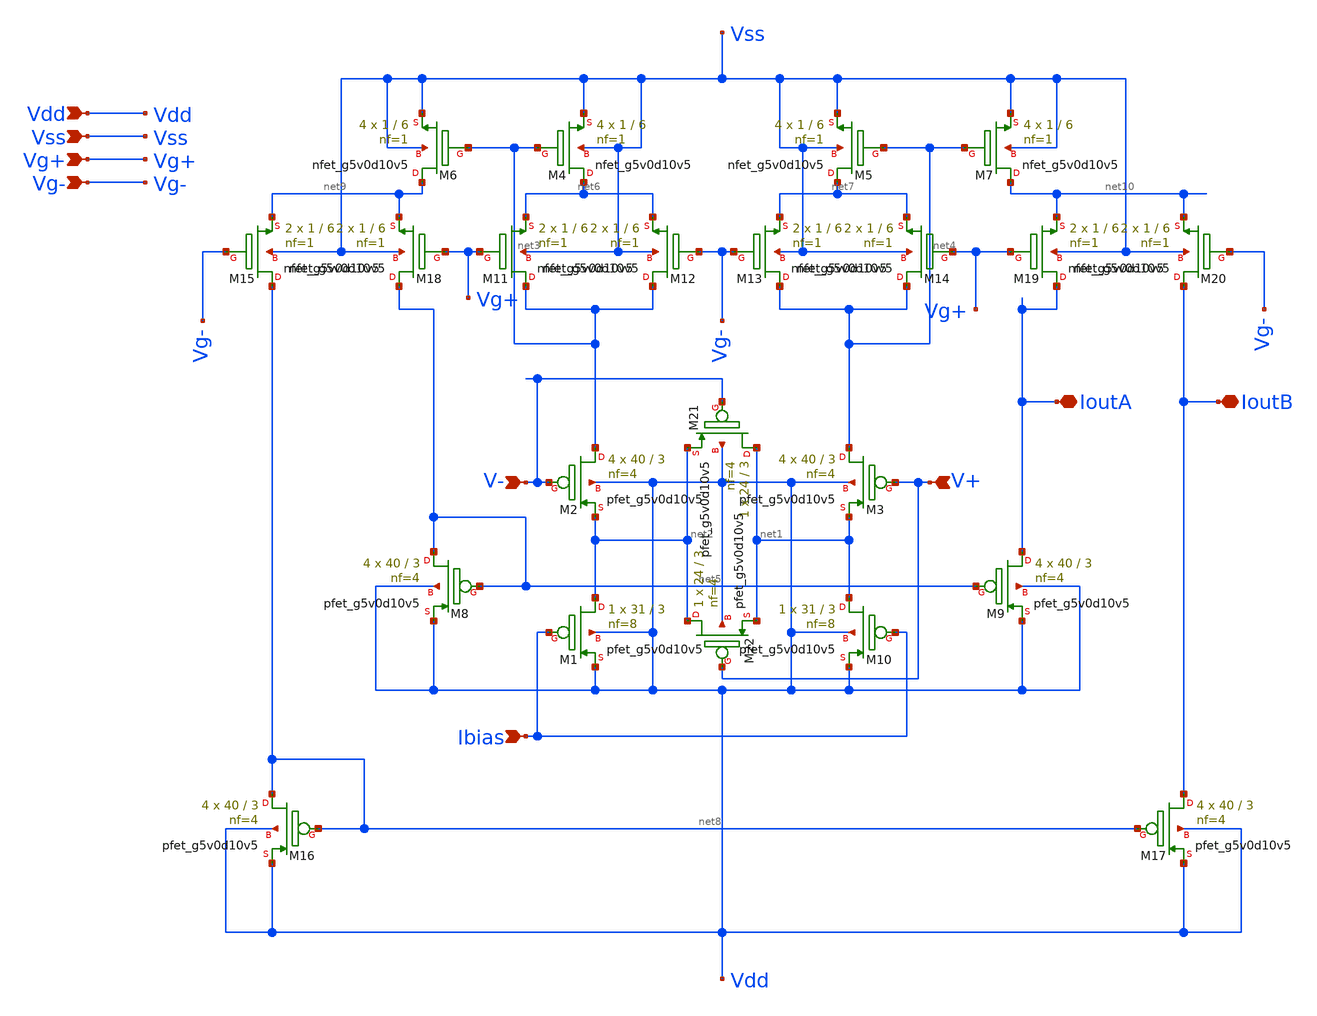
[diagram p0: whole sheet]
** sch_path: xschem/Gm_C_LPF.sch
**.subckt Gm_C_LPF V- V+ Vdd Vss Ibias Vg- Vg+ IoutA IoutB
*.ipin V-
*.ipin V+
*.ipin Vdd
*.ipin Vss
*.ipin Ibias
*.ipin Vg-
*.ipin Vg+
*.iopin IoutA
*.iopin IoutB
XM1 net2 Ibias Vdd Vdd sky130_fd_pr__pfet_g5v0d10v5 L=3 W=31 nf=8 ad='int((8 + 1)/2) * 31 / 8 * 0.29'
+ as='int((8 + 2)/2) * 31 / 8 * 0.29' pd='2*int((8 + 1)/2) * (31 / 8 + 0.29)' ps='2*int((8 + 2)/2) * (31 / 8 + 0.29)'
+ nrd='0.29 / 31 ' nrs='0.29 / 31 ' sa=0 sb=0 sd=0 mult=1 m=1
XM2 net3 V- net2 Vdd sky130_fd_pr__pfet_g5v0d10v5 L=3 W=40 nf=4 ad='int((4 + 1)/2) * 40 / 4 * 0.29' as='int((4 + 2)/2) * 40 / 4 * 0.29'
+ pd='2*int((4 + 1)/2) * (40 / 4 + 0.29)' ps='2*int((4 + 2)/2) * (40 / 4 + 0.29)' nrd='0.29 / 40 ' nrs='0.29 / 40 '
+ sa=0 sb=0 sd=0 mult=4 m=4
XM3 net4 V+ net1 Vdd sky130_fd_pr__pfet_g5v0d10v5 L=3 W=40 nf=4 ad='int((4 + 1)/2) * 40 / 4 * 0.29' as='int((4 + 2)/2) * 40 / 4 * 0.29'
+ pd='2*int((4 + 1)/2) * (40 / 4 + 0.29)' ps='2*int((4 + 2)/2) * (40 / 4 + 0.29)' nrd='0.29 / 40 ' nrs='0.29 / 40 '
+ sa=0 sb=0 sd=0 mult=4 m=4
XM4 net6 net3 Vss Vss sky130_fd_pr__nfet_g5v0d10v5 L=6 W=1 nf=1 ad='int((1 + 1)/2) * 1 / 1 * 0.29' as='int((1 + 2)/2) * 1 / 1 * 0.29'
+ pd='2*int((1 + 1)/2) * (1 / 1 + 0.29)' ps='2*int((1 + 2)/2) * (1 / 1 + 0.29)' nrd='0.29 / 1 ' nrs='0.29 / 1 '
+ sa=0 sb=0 sd=0 mult=4 m=4
XM5 net7 net4 Vss Vss sky130_fd_pr__nfet_g5v0d10v5 L=6 W=1 nf=1 ad='int((1 + 1)/2) * 1 / 1 * 0.29' as='int((1 + 2)/2) * 1 / 1 * 0.29'
+ pd='2*int((1 + 1)/2) * (1 / 1 + 0.29)' ps='2*int((1 + 2)/2) * (1 / 1 + 0.29)' nrd='0.29 / 1 ' nrs='0.29 / 1 '
+ sa=0 sb=0 sd=0 mult=4 m=4
XM6 net9 net3 Vss Vss sky130_fd_pr__nfet_g5v0d10v5 L=6 W=1 nf=1 ad='int((1 + 1)/2) * 1 / 1 * 0.29' as='int((1 + 2)/2) * 1 / 1 * 0.29'
+ pd='2*int((1 + 1)/2) * (1 / 1 + 0.29)' ps='2*int((1 + 2)/2) * (1 / 1 + 0.29)' nrd='0.29 / 1 ' nrs='0.29 / 1 '
+ sa=0 sb=0 sd=0 mult=4 m=4
XM7 net10 net4 Vss Vss sky130_fd_pr__nfet_g5v0d10v5 L=6 W=1 nf=1 ad='int((1 + 1)/2) * 1 / 1 * 0.29' as='int((1 + 2)/2) * 1 / 1 * 0.29'
+ pd='2*int((1 + 1)/2) * (1 / 1 + 0.29)' ps='2*int((1 + 2)/2) * (1 / 1 + 0.29)' nrd='0.29 / 1 ' nrs='0.29 / 1 '
+ sa=0 sb=0 sd=0 mult=4 m=4
XM8 net5 net5 Vdd Vdd sky130_fd_pr__pfet_g5v0d10v5 L=3 W=40 nf=4 ad='int((4 + 1)/2) * 40 / 4 * 0.29'
+ as='int((4 + 2)/2) * 40 / 4 * 0.29' pd='2*int((4 + 1)/2) * (40 / 4 + 0.29)' ps='2*int((4 + 2)/2) * (40 / 4 + 0.29)'
+ nrd='0.29 / 40 ' nrs='0.29 / 40 ' sa=0 sb=0 sd=0 mult=4 m=4
XM9 IoutA net5 Vdd Vdd sky130_fd_pr__pfet_g5v0d10v5 L=3 W=40 nf=4 ad='int((4 + 1)/2) * 40 / 4 * 0.29'
+ as='int((4 + 2)/2) * 40 / 4 * 0.29' pd='2*int((4 + 1)/2) * (40 / 4 + 0.29)' ps='2*int((4 + 2)/2) * (40 / 4 + 0.29)'
+ nrd='0.29 / 40 ' nrs='0.29 / 40 ' sa=0 sb=0 sd=0 mult=4 m=4
XM10 net1 Ibias Vdd Vdd sky130_fd_pr__pfet_g5v0d10v5 L=3 W=31 nf=8 ad='int((8 + 1)/2) * 31 / 8 * 0.29'
+ as='int((8 + 2)/2) * 31 / 8 * 0.29' pd='2*int((8 + 1)/2) * (31 / 8 + 0.29)' ps='2*int((8 + 2)/2) * (31 / 8 + 0.29)'
+ nrd='0.29 / 31 ' nrs='0.29 / 31 ' sa=0 sb=0 sd=0 mult=1 m=1
XM11 net3 Vg+ net6 Vss sky130_fd_pr__nfet_g5v0d10v5 L=6 W=1 nf=1 ad='int((1 + 1)/2) * 1 / 1 * 0.29' as='int((1 + 2)/2) * 1 / 1 * 0.29'
+ pd='2*int((1 + 1)/2) * (1 / 1 + 0.29)' ps='2*int((1 + 2)/2) * (1 / 1 + 0.29)' nrd='0.29 / 1 ' nrs='0.29 / 1 '
+ sa=0 sb=0 sd=0 mult=2 m=2
XM12 net3 Vg- net6 Vss sky130_fd_pr__nfet_g5v0d10v5 L=6 W=1 nf=1 ad='int((1 + 1)/2) * 1 / 1 * 0.29' as='int((1 + 2)/2) * 1 / 1 * 0.29'
+ pd='2*int((1 + 1)/2) * (1 / 1 + 0.29)' ps='2*int((1 + 2)/2) * (1 / 1 + 0.29)' nrd='0.29 / 1 ' nrs='0.29 / 1 '
+ sa=0 sb=0 sd=0 mult=2 m=2
XM13 net4 Vg- net7 Vss sky130_fd_pr__nfet_g5v0d10v5 L=6 W=1 nf=1 ad='int((1 + 1)/2) * 1 / 1 * 0.29' as='int((1 + 2)/2) * 1 / 1 * 0.29'
+ pd='2*int((1 + 1)/2) * (1 / 1 + 0.29)' ps='2*int((1 + 2)/2) * (1 / 1 + 0.29)' nrd='0.29 / 1 ' nrs='0.29 / 1 '
+ sa=0 sb=0 sd=0 mult=2 m=2
XM14 net4 Vg+ net7 Vss sky130_fd_pr__nfet_g5v0d10v5 L=6 W=1 nf=1 ad='int((1 + 1)/2) * 1 / 1 * 0.29' as='int((1 + 2)/2) * 1 / 1 * 0.29'
+ pd='2*int((1 + 1)/2) * (1 / 1 + 0.29)' ps='2*int((1 + 2)/2) * (1 / 1 + 0.29)' nrd='0.29 / 1 ' nrs='0.29 / 1 '
+ sa=0 sb=0 sd=0 mult=2 m=2
XM16 net8 net8 Vdd Vdd sky130_fd_pr__pfet_g5v0d10v5 L=3 W=40 nf=4 ad='int((4 + 1)/2) * 40 / 4 * 0.29'
+ as='int((4 + 2)/2) * 40 / 4 * 0.29' pd='2*int((4 + 1)/2) * (40 / 4 + 0.29)' ps='2*int((4 + 2)/2) * (40 / 4 + 0.29)'
+ nrd='0.29 / 40 ' nrs='0.29 / 40 ' sa=0 sb=0 sd=0 mult=4 m=4
XM17 IoutB net8 Vdd Vdd sky130_fd_pr__pfet_g5v0d10v5 L=3 W=40 nf=4 ad='int((4 + 1)/2) * 40 / 4 * 0.29'
+ as='int((4 + 2)/2) * 40 / 4 * 0.29' pd='2*int((4 + 1)/2) * (40 / 4 + 0.29)' ps='2*int((4 + 2)/2) * (40 / 4 + 0.29)'
+ nrd='0.29 / 40 ' nrs='0.29 / 40 ' sa=0 sb=0 sd=0 mult=4 m=4
XM15 net8 Vg- net9 Vss sky130_fd_pr__nfet_g5v0d10v5 L=6 W=1 nf=1 ad='int((1 + 1)/2) * 1 / 1 * 0.29' as='int((1 + 2)/2) * 1 / 1 * 0.29'
+ pd='2*int((1 + 1)/2) * (1 / 1 + 0.29)' ps='2*int((1 + 2)/2) * (1 / 1 + 0.29)' nrd='0.29 / 1 ' nrs='0.29 / 1 '
+ sa=0 sb=0 sd=0 mult=2 m=2
XM18 net5 Vg+ net9 Vss sky130_fd_pr__nfet_g5v0d10v5 L=6 W=1 nf=1 ad='int((1 + 1)/2) * 1 / 1 * 0.29' as='int((1 + 2)/2) * 1 / 1 * 0.29'
+ pd='2*int((1 + 1)/2) * (1 / 1 + 0.29)' ps='2*int((1 + 2)/2) * (1 / 1 + 0.29)' nrd='0.29 / 1 ' nrs='0.29 / 1 '
+ sa=0 sb=0 sd=0 mult=2 m=2
XM19 IoutA Vg+ net10 Vss sky130_fd_pr__nfet_g5v0d10v5 L=6 W=1 nf=1 ad='int((1 + 1)/2) * 1 / 1 * 0.29'
+ as='int((1 + 2)/2) * 1 / 1 * 0.29' pd='2*int((1 + 1)/2) * (1 / 1 + 0.29)' ps='2*int((1 + 2)/2) * (1 / 1 + 0.29)'
+ nrd='0.29 / 1 ' nrs='0.29 / 1 ' sa=0 sb=0 sd=0 mult=2 m=2
XM20 IoutB Vg- net10 Vss sky130_fd_pr__nfet_g5v0d10v5 L=6 W=1 nf=1 ad='int((1 + 1)/2) * 1 / 1 * 0.29'
+ as='int((1 + 2)/2) * 1 / 1 * 0.29' pd='2*int((1 + 1)/2) * (1 / 1 + 0.29)' ps='2*int((1 + 2)/2) * (1 / 1 + 0.29)'
+ nrd='0.29 / 1 ' nrs='0.29 / 1 ' sa=0 sb=0 sd=0 mult=2 m=2
XM21 net1 V- net2 Vdd sky130_fd_pr__pfet_g5v0d10v5 L=3 W=24 nf=4 ad='int((4 + 1)/2) * 24 / 4 * 0.29'
+ as='int((4 + 2)/2) * 24 / 4 * 0.29' pd='2*int((4 + 1)/2) * (24 / 4 + 0.29)' ps='2*int((4 + 2)/2) * (24 / 4 + 0.29)'
+ nrd='0.29 / 24 ' nrs='0.29 / 24 ' sa=0 sb=0 sd=0 mult=1 m=1
XM22 net2 V+ net1 Vdd sky130_fd_pr__pfet_g5v0d10v5 L=3 W=24 nf=4 ad='int((4 + 1)/2) * 24 / 4 * 0.29'
+ as='int((4 + 2)/2) * 24 / 4 * 0.29' pd='2*int((4 + 1)/2) * (24 / 4 + 0.29)' ps='2*int((4 + 2)/2) * (24 / 4 + 0.29)'
+ nrd='0.29 / 24 ' nrs='0.29 / 24 ' sa=0 sb=0 sd=0 mult=1 m=1
**.ends
.end
